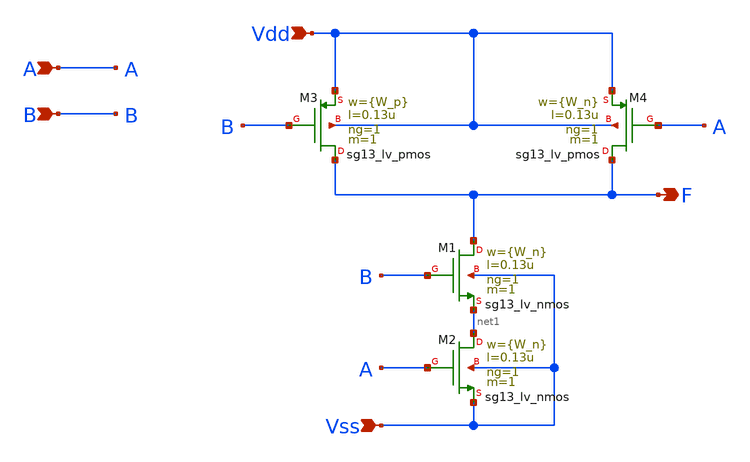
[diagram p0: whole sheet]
** sch_path: xschem/LogicGates/NAND.sch
**.subckt NAND Vss A B Vdd F
*.ipin Vss
*.ipin A
*.ipin B
*.ipin Vdd
*.opin F
XM1 F B net1 Vss sg13_lv_nmos w={W_n} l=0.13u ng=1 m=1 mm_ok=1
XM2 net1 A Vss Vss sg13_lv_nmos w={W_n} l=0.13u ng=1 m=1 mm_ok=1
XM3 F B Vdd Vdd sg13_lv_pmos w={W_p} l=0.13u ng=1 m=1 mm_ok=1
XM4 F A Vdd Vdd sg13_lv_pmos w={W_n} l=0.13u ng=1 m=1 mm_ok=1
**.ends
.end
